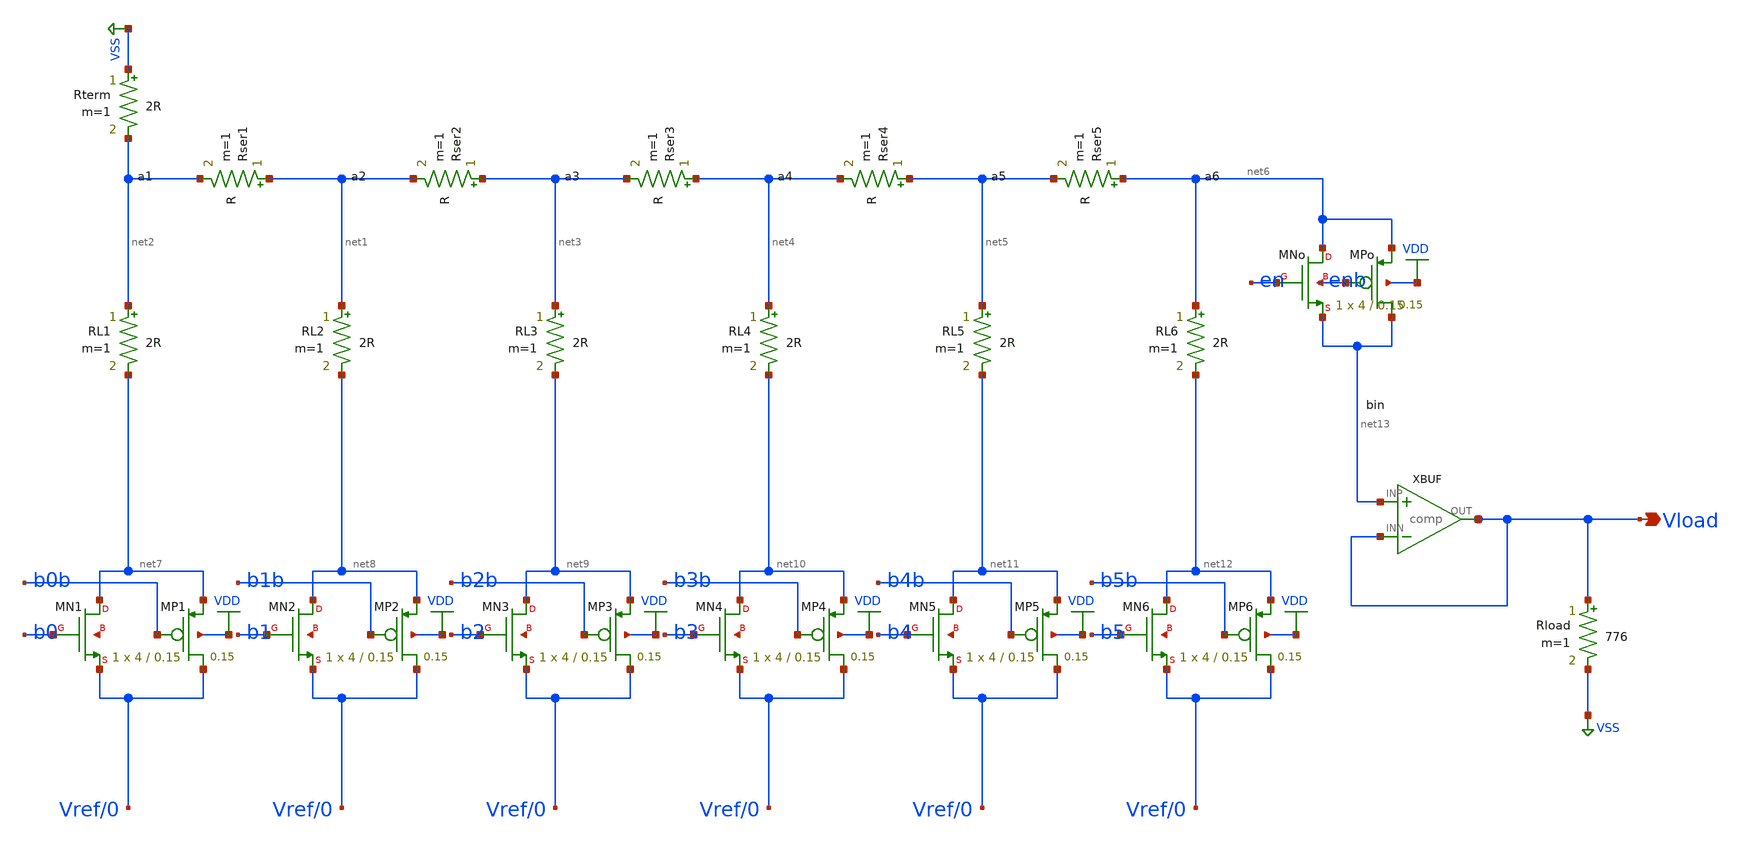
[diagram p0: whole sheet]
** sch_path: eda/hero/schematics/r2r_dac.sch
**.subckt r2r_dac Vload
*.opin Vload
Rser1 net1 net2 R m=1
Rser2 net3 net1 R m=1
Rser3 net4 net3 R m=1
Rser4 net5 net4 R m=1
Rser5 net6 net5 R m=1
Rterm VSS net2 2R m=1
RL1 net2 net7 2R m=1
XMN1 net7 b0 Vref/0 net14 sky130_fd_pr__sky130_fd_pr__nfet_01v8 L=0.15 W=4 nrd='0.29 / W' nrs='0.29 / W'
+ sa=0 sb=0 sd=0 mult=1 m=1
XMP1 Vref/0 b0b net7 VDD sky130_fd_pr__sky130_fd_pr__pfet_01v8 L=0.15 W=8 nrd='0.29 / W' nrs='0.29 / W'
+ sa=0 sb=0 sd=0 mult=1 m=1
RL2 net1 net8 2R m=1
XMN2 net8 b1 Vref/0 net15 sky130_fd_pr__sky130_fd_pr__nfet_01v8 L=0.15 W=4 nrd='0.29 / W' nrs='0.29 / W'
+ sa=0 sb=0 sd=0 mult=1 m=1
XMP2 Vref/0 b1b net8 VDD sky130_fd_pr__sky130_fd_pr__pfet_01v8 L=0.15 W=8 nrd='0.29 / W' nrs='0.29 / W'
+ sa=0 sb=0 sd=0 mult=1 m=1
RL3 net3 net9 2R m=1
XMN3 net9 b2 Vref/0 net16 sky130_fd_pr__sky130_fd_pr__nfet_01v8 L=0.15 W=4 nrd='0.29 / W' nrs='0.29 / W'
+ sa=0 sb=0 sd=0 mult=1 m=1
XMP3 Vref/0 b2b net9 VDD sky130_fd_pr__sky130_fd_pr__pfet_01v8 L=0.15 W=8 nrd='0.29 / W' nrs='0.29 / W'
+ sa=0 sb=0 sd=0 mult=1 m=1
RL4 net4 net10 2R m=1
XMN4 net10 b3 Vref/0 net17 sky130_fd_pr__sky130_fd_pr__nfet_01v8 L=0.15 W=4 nrd='0.29 / W' nrs='0.29 / W'
+ sa=0 sb=0 sd=0 mult=1 m=1
XMP4 Vref/0 b3b net10 VDD sky130_fd_pr__sky130_fd_pr__pfet_01v8 L=0.15 W=8 nrd='0.29 / W' nrs='0.29 / W'
+ sa=0 sb=0 sd=0 mult=1 m=1
RL5 net5 net11 2R m=1
XMN5 net11 b4 Vref/0 net18 sky130_fd_pr__sky130_fd_pr__nfet_01v8 L=0.15 W=4 nrd='0.29 / W' nrs='0.29 / W'
+ sa=0 sb=0 sd=0 mult=1 m=1
XMP5 Vref/0 b4b net11 VDD sky130_fd_pr__sky130_fd_pr__pfet_01v8 L=0.15 W=8 nrd='0.29 / W' nrs='0.29 / W'
+ sa=0 sb=0 sd=0 mult=1 m=1
RL6 net6 net12 2R m=1
XMN6 net12 b5 Vref/0 net19 sky130_fd_pr__sky130_fd_pr__nfet_01v8 L=0.15 W=4 nrd='0.29 / W' nrs='0.29 / W'
+ sa=0 sb=0 sd=0 mult=1 m=1
XMP6 Vref/0 b5b net12 VDD sky130_fd_pr__sky130_fd_pr__pfet_01v8 L=0.15 W=8 nrd='0.29 / W' nrs='0.29 / W'
+ sa=0 sb=0 sd=0 mult=1 m=1
XMNo net6 en net13 enb sky130_fd_pr__sky130_fd_pr__nfet_01v8 L=0.15 W=4 nrd='0.29 / W' nrs='0.29 / W'
+ sa=0 sb=0 sd=0 mult=1 m=1
XMPo net13 enb net6 VDD sky130_fd_pr__sky130_fd_pr__pfet_01v8 L=0.15 W=8 nrd='0.29 / W' nrs='0.29 / W'
+ sa=0 sb=0 sd=0 mult=1 m=1
Rload Vload VSS 776 m=1
**.ends
.GLOBAL VSS
.GLOBAL VDD
.end
